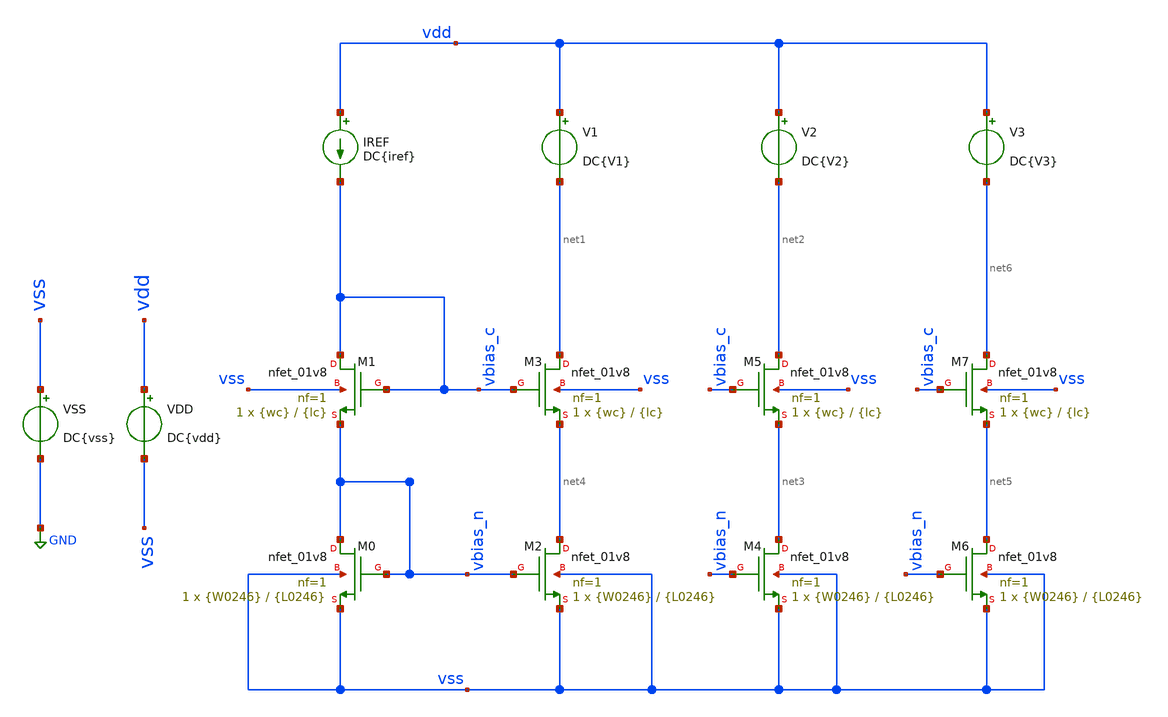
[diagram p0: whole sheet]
** sch_path: TP2/tp2_3a.sch
**.subckt tp2_3a
XM0 vbias_n vbias_n vss vss sky130_fd_pr__nfet_01v8 L={L0246} W={W0246} nf=1 ad='int((nf+1)/2) * W/nf * 0.29'
+ as='int((nf+2)/2) * W/nf * 0.29' pd='2*int((nf+1)/2) * (W/nf + 0.29)' ps='2*int((nf+2)/2) * (W/nf + 0.29)'
+ nrd='0.29 / W' nrs='0.29 / W' sa=0 sb=0 sd=0 mult=1 m=1
XM2 net4 vbias_n vss vss sky130_fd_pr__nfet_01v8 L={L0246} W={W0246} nf=1 ad='int((nf+1)/2) * W/nf * 0.29'
+ as='int((nf+2)/2) * W/nf * 0.29' pd='2*int((nf+1)/2) * (W/nf + 0.29)' ps='2*int((nf+2)/2) * (W/nf + 0.29)'
+ nrd='0.29 / W' nrs='0.29 / W' sa=0 sb=0 sd=0 mult=1 m=1
IREF vdd vbias_c DC{iref}
VSS vss GND DC{vss}
VDD vdd vss DC{vdd}
XM3 net1 vbias_c net4 vss sky130_fd_pr__nfet_01v8 L={lc} W={wc} nf=1 ad='int((nf+1)/2) * W/nf * 0.29'
+ as='int((nf+2)/2) * W/nf * 0.29' pd='2*int((nf+1)/2) * (W/nf + 0.29)' ps='2*int((nf+2)/2) * (W/nf + 0.29)'
+ nrd='0.29 / W' nrs='0.29 / W' sa=0 sb=0 sd=0 mult=1 m=1
V1 vdd net1 DC{V1}
V2 vdd net2 DC{V2}
XM4 net3 vbias_n vss vss sky130_fd_pr__nfet_01v8 L={L0246} W={W0246} nf=1 ad='int((nf+1)/2) * W/nf * 0.29'
+ as='int((nf+2)/2) * W/nf * 0.29' pd='2*int((nf+1)/2) * (W/nf + 0.29)' ps='2*int((nf+2)/2) * (W/nf + 0.29)'
+ nrd='0.29 / W' nrs='0.29 / W' sa=0 sb=0 sd=0 mult=1 m=1
V3 vdd net6 DC{V3}
XM1 vbias_c vbias_c vbias_n vss sky130_fd_pr__nfet_01v8 L={lc} W={wc} nf=1 ad='int((nf+1)/2) * W/nf * 0.29'
+ as='int((nf+2)/2) * W/nf * 0.29' pd='2*int((nf+1)/2) * (W/nf + 0.29)' ps='2*int((nf+2)/2) * (W/nf + 0.29)'
+ nrd='0.29 / W' nrs='0.29 / W' sa=0 sb=0 sd=0 mult=1 m=1
XM6 net5 vbias_n vss vss sky130_fd_pr__nfet_01v8 L={L0246} W={W0246} nf=1 ad='int((nf+1)/2) * W/nf * 0.29'
+ as='int((nf+2)/2) * W/nf * 0.29' pd='2*int((nf+1)/2) * (W/nf + 0.29)' ps='2*int((nf+2)/2) * (W/nf + 0.29)'
+ nrd='0.29 / W' nrs='0.29 / W' sa=0 sb=0 sd=0 mult=1 m=1
XM7 net6 vbias_c net5 vss sky130_fd_pr__nfet_01v8 L={lc} W={wc} nf=1 ad='int((nf+1)/2) * W/nf * 0.29'
+ as='int((nf+2)/2) * W/nf * 0.29' pd='2*int((nf+1)/2) * (W/nf + 0.29)' ps='2*int((nf+2)/2) * (W/nf + 0.29)'
+ nrd='0.29 / W' nrs='0.29 / W' sa=0 sb=0 sd=0 mult=1 m=1
XM5 net2 vbias_c net3 vss sky130_fd_pr__nfet_01v8 L={lc} W={wc} nf=1 ad='int((nf+1)/2) * W/nf * 0.29'
+ as='int((nf+2)/2) * W/nf * 0.29' pd='2*int((nf+1)/2) * (W/nf + 0.29)' ps='2*int((nf+2)/2) * (W/nf + 0.29)'
+ nrd='0.29 / W' nrs='0.29 / W' sa=0 sb=0 sd=0 mult=1 m=1
**** begin user architecture code



* Parameters
.param vdd = 1.8
.param vss = 0.0
.param V1 = 0.6
.param V2 = 0.9
.param V3 = 1.2
.param iref = 200u
.param L0246 = 0.15
.param lc = 0.9
.param W0246 = 5
.param wc = 20
.options TEMPS = 27.0

* Models
.lib ~/skywater/skywater-pdk/libraries/sky130_fd_pr_ngspice/latest/models/corners/sky130.lib TT

* Data to save
.save all  @M.XM0.msky130_fd_pr__nfet_01v8[id]  @M.XM0.msky130_fd_pr__nfet_01v8[gm]  @M.XM0.msky130_fd_pr__nfet_01v8[vds]  @M.XM0.msky130_fd_pr__nfet_01v8[vgs]  @M.XM0.msky130_fd_pr__nfet_01v8[w]  @M.XM0.msky130_fd_pr__nfet_01v8[vth]  @M.XM0.msky130_fd_pr__nfet_01v8[vdsat]  @M.XM1.msky130_fd_pr__nfet_01v8[id]  @M.XM1.msky130_fd_pr__nfet_01v8[gm]  @M.XM1.msky130_fd_pr__nfet_01v8[vds]  @M.XM1.msky130_fd_pr__nfet_01v8[vgs]  @M.XM1.msky130_fd_pr__nfet_01v8[w]  @M.XM1.msky130_fd_pr__nfet_01v8[vth]  @M.XM1.msky130_fd_pr__nfet_01v8[vdsat]  @M.XM2.msky130_fd_pr__nfet_01v8[id]  @M.XM2.msky130_fd_pr__nfet_01v8[gm]  @M.XM2.msky130_fd_pr__nfet_01v8[vds]  @M.XM2.msky130_fd_pr__nfet_01v8[vgs]  @M.XM2.msky130_fd_pr__nfet_01v8[w]  @M.XM2.msky130_fd_pr__nfet_01v8[vth]  @M.XM2.msky130_fd_pr__nfet_01v8[vdsat]  @M.XM3.msky130_fd_pr__nfet_01v8[id]  @M.XM3.msky130_fd_pr__nfet_01v8[gm]  @M.XM3.msky130_fd_pr__nfet_01v8[vds]  @M.XM3.msky130_fd_pr__nfet_01v8[vgs]  @M.XM3.msky130_fd_pr__nfet_01v8[w]  @M.XM3.msky130_fd_pr__nfet_01v8[vth]  @M.XM3.msky130_fd_pr__nfet_01v8[vdsat]  @M.XM4.msky130_fd_pr__nfet_01v8[id]  @M.XM4.msky130_fd_pr__nfet_01v8[gm]  @M.XM4.msky130_fd_pr__nfet_01v8[vds]  @M.XM4.msky130_fd_pr__nfet_01v8[vgs]  @M.XM4.msky130_fd_pr__nfet_01v8[w]  @M.XM4.msky130_fd_pr__nfet_01v8[vth]  @M.XM4.msky130_fd_pr__nfet_01v8[vdsat]  @M.XM5.msky130_fd_pr__nfet_01v8[id]  @M.XM5.msky130_fd_pr__nfet_01v8[gm]  @M.XM5.msky130_fd_pr__nfet_01v8[vds]  @M.XM5.msky130_fd_pr__nfet_01v8[vgs]  @M.XM5.msky130_fd_pr__nfet_01v8[w]  @M.XM5.msky130_fd_pr__nfet_01v8[vth]  @M.XM5.msky130_fd_pr__nfet_01v8[vdsat]  @M.XM6.msky130_fd_pr__nfet_01v8[id]  @M.XM6.msky130_fd_pr__nfet_01v8[gm]  @M.XM6.msky130_fd_pr__nfet_01v8[vds]  @M.XM6.msky130_fd_pr__nfet_01v8[vgs]  @M.XM6.msky130_fd_pr__nfet_01v8[w]  @M.XM6.msky130_fd_pr__nfet_01v8[vth]  @M.XM6.msky130_fd_pr__nfet_01v8[vdsat]  @M.XM7.msky130_fd_pr__nfet_01v8[id]  @M.XM7.msky130_fd_pr__nfet_01v8[gm]  @M.XM7.msky130_fd_pr__nfet_01v8[vds]  @M.XM7.msky130_fd_pr__nfet_01v8[vgs]  @M.XM7.msky130_fd_pr__nfet_01v8[w]  @M.XM7.msky130_fd_pr__nfet_01v8[vth]  @M.XM7.msky130_fd_pr__nfet_01v8[vdsat]


* Simulation
.control
  op
  save all
  unset filetype
  write tp2_3a.raw

.endc

.end


**** end user architecture code
**.ends
.GLOBAL GND
.end
